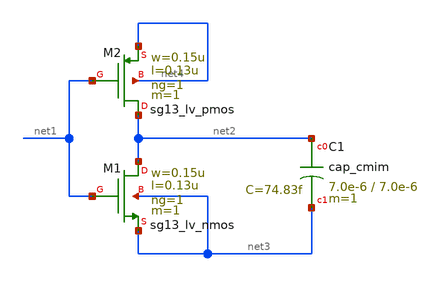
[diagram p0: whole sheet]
** sch_path: current_generator/analog/inverter_test.sch
**.subckt inverter_test
XM1 net2 net1 net3 net3 sg13_lv_nmos w=0.15u l=0.13u ng=1 m=1 mm_ok=1
XM2 net2 net1 net4 net4 sg13_lv_pmos w=0.15u l=0.13u ng=1 m=1 mm_ok=1
XC1 net2 net3 cap_cmim w=7.0e-6 l=7.0e-6 m=1 mm_ok=1
**.ends
.end
